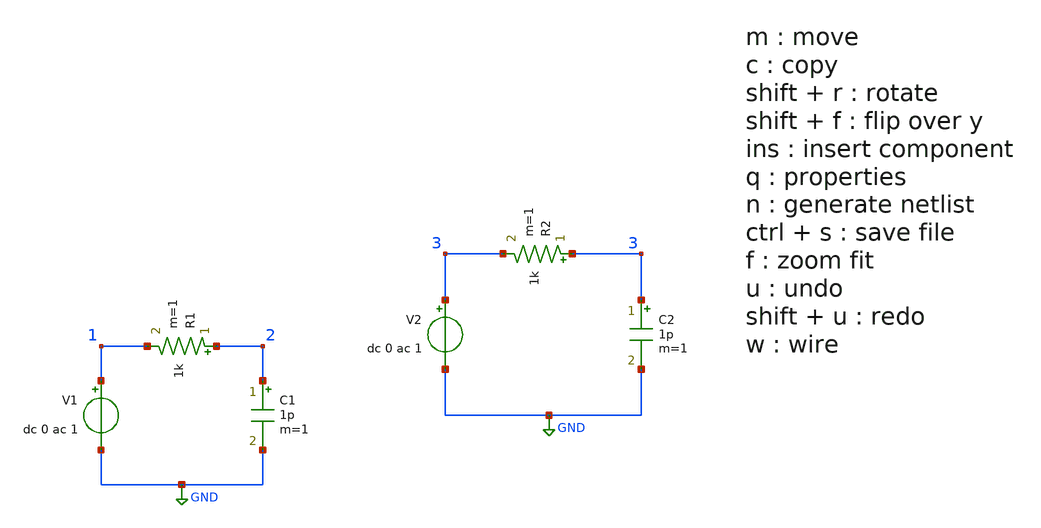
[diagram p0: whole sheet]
** sch_path: circuitos/exemplo01.sch
**.subckt exemplo01
C1 2 GND 1p m=1
R1 2 1 1k m=1
V1 1 GND dc 0 ac 1
R2 3 3 1k m=1
C2 3 GND 1p m=1
V2 3 GND dc 0 ac 1
**** begin user architecture code

.ac lin 1001 100 100Meg

**** end user architecture code
**.ends
.GLOBAL GND
.end
